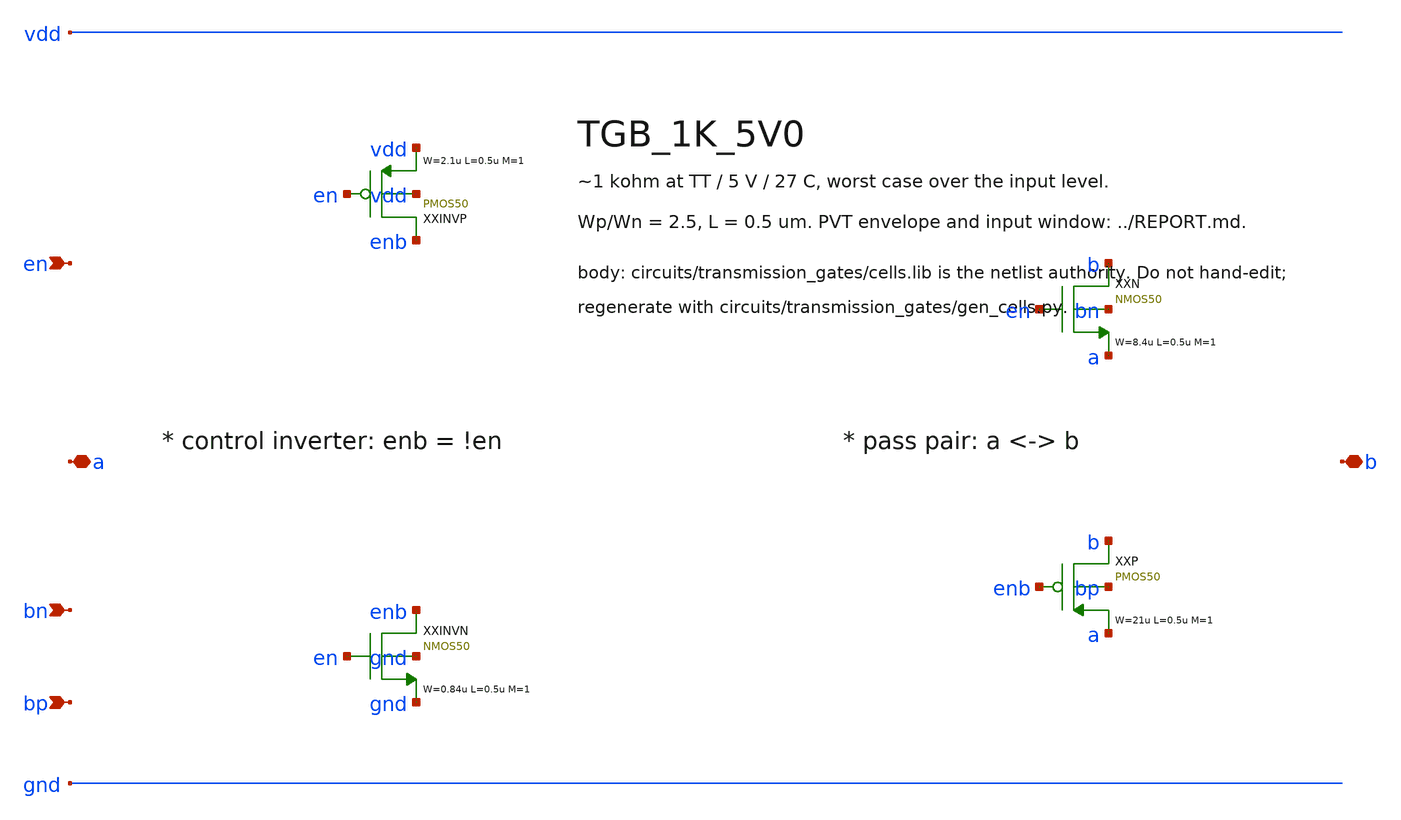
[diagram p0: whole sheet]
** sch_path: xschem/transmission_gates/TGB_1K_5V0.sch
**.subckt TGB_1K_5V0 a b en bn bp
*.iopin a
*.iopin b
*.ipin en
*.ipin bn
*.ipin bp
XXINVP enb en vdd vdd PMOS50 W=2.1u L=0.5u M=1 MM_SIGMA=0
XXINVN enb en gnd gnd NMOS50 W=0.84u L=0.5u M=1 MM_SIGMA=0
XXN b en a bn NMOS50 W=8.4u L=0.5u M=1 MM_SIGMA=0
XXP b enb a bp PMOS50 W=21u L=0.5u M=1 MM_SIGMA=0
**.ends
.end
